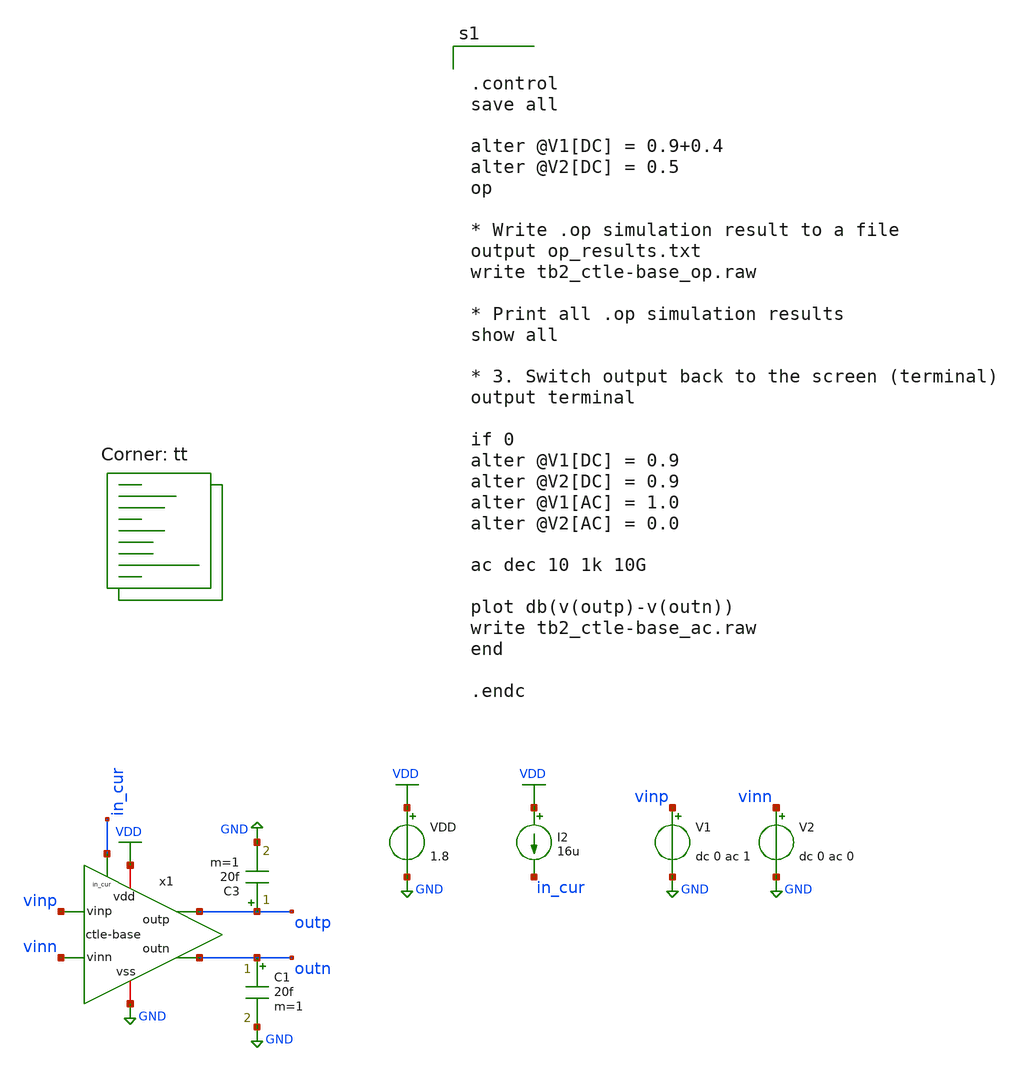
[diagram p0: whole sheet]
** sch_path: CTLE/tb2_ctle-base.sch
**.subckt tb2_ctle-base
x1 VDD GND outp outn vinn vinp in_cur ctle-base
VDD VDD GND 1.8
V1 vinp GND dc 0 ac 1
V2 vinn GND dc 0 ac 0
I2 VDD in_cur 16u
C3 outp GND 20f m=1
C1 outn GND 20f m=1
**** begin user architecture code
.lib $::SKYWATER_MODELS/sky130.lib.spice tt


.control
save all

alter @V1[DC] = 0.9+0.4
alter @V2[DC] = 0.5
op

* Write .op simulation result to a file
output op_results.txt
write tb2_ctle-base_op.raw

* Print all .op simulation results
show all

* 3. Switch output back to the screen (terminal)
output terminal

if 0
alter @V1[DC] = 0.9
alter @V2[DC] = 0.9
alter @V1[AC] = 1.0
alter @V2[AC] = 0.0

ac dec 10 1k 10G

plot db(v(outp)-v(outn))
write tb2_ctle-base_ac.raw
end

.endc

**** end user architecture code
**.ends

* expanding   symbol:  /foss/designs/Teknofest/afe-icdec-teknofest-2026/CTLE/ctle-base.sym # of
*+ pins=7
** sym_path: CTLE/ctle-base.sym
** sch_path: CTLE/ctle-base.sch
.subckt ctle-base vdd vss outp outn vinn vinp in_cur
*.iopin vdd
*.iopin vss
*.ipin vinp
*.ipin vinn
*.opin outn
*.opin outp
*.ipin in_cur
XM1 outn vinp vsm1 vsm1 sky130_fd_pr__nfet_01v8 L=0.15 W=12.5 nf=1 ad='int((nf+1)/2) * W/nf * 0.29' as='int((nf+2)/2) * W/nf * 0.29'
+ pd='2*int((nf+1)/2) * (W/nf + 0.29)' ps='2*int((nf+2)/2) * (W/nf + 0.29)' nrd='0.29 / W' nrs='0.29 / W'
+ sa=0 sb=0 sd=0 mult=1 m=1
XM2 outp vinn vsm2 vsm2 sky130_fd_pr__nfet_01v8 L=0.15 W=12.5 nf=1 ad='int((nf+1)/2) * W/nf * 0.29' as='int((nf+2)/2) * W/nf * 0.29'
+ pd='2*int((nf+1)/2) * (W/nf + 0.29)' ps='2*int((nf+2)/2) * (W/nf + 0.29)' nrd='0.29 / W' nrs='0.29 / W'
+ sa=0 sb=0 sd=0 mult=1 m=1
XC1 vsm1 vsm2 sky130_fd_pr__cap_mim_m3_1 W=7.5 L=7.5 MF=1 m=1
XM5 in_cur in_cur vss vss sky130_fd_pr__nfet_01v8 L=0.5 W=1 nf=1 ad='int((nf+1)/2) * W/nf * 0.29' as='int((nf+2)/2) * W/nf * 0.29'
+ pd='2*int((nf+1)/2) * (W/nf + 0.29)' ps='2*int((nf+2)/2) * (W/nf + 0.29)' nrd='0.29 / W' nrs='0.29 / W'
+ sa=0 sb=0 sd=0 mult=1 m=1
XM6 vsm1 in_cur vss vss sky130_fd_pr__nfet_01v8 L=0.5 W=21.88 nf=1 ad='int((nf+1)/2) * W/nf * 0.29' as='int((nf+2)/2) * W/nf * 0.29'
+ pd='2*int((nf+1)/2) * (W/nf + 0.29)' ps='2*int((nf+2)/2) * (W/nf + 0.29)' nrd='0.29 / W' nrs='0.29 / W'
+ sa=0 sb=0 sd=0 mult=1 m=1
XM7 vsm2 in_cur vss vss sky130_fd_pr__nfet_01v8 L=0.5 W=21.88 nf=1 ad='int((nf+1)/2) * W/nf * 0.29' as='int((nf+2)/2) * W/nf * 0.29'
+ pd='2*int((nf+1)/2) * (W/nf + 0.29)' ps='2*int((nf+2)/2) * (W/nf + 0.29)' nrd='0.29 / W' nrs='0.29 / W'
+ sa=0 sb=0 sd=0 mult=1 m=1
XR3 vsm1 vsm2 vss sky130_fd_pr__res_xhigh_po_0p35 L=0.45 mult=1 m=1
XR1 vdd outn vss sky130_fd_pr__res_xhigh_po_0p35 L=0.45 mult=1 m=1
XR2 vdd outp vss sky130_fd_pr__res_xhigh_po_0p35 L=0.45 mult=1 m=1
.ends

.GLOBAL GND
.GLOBAL VDD
.end
